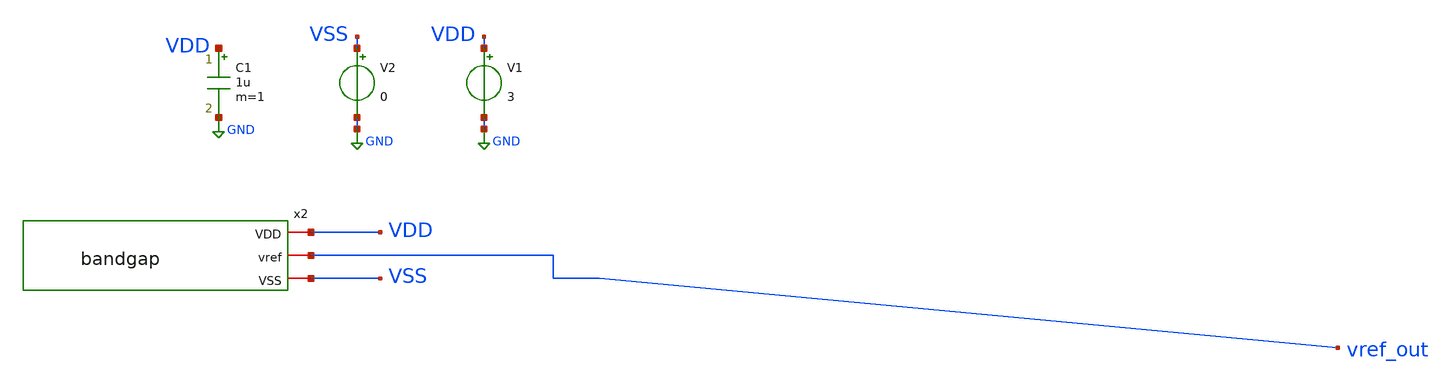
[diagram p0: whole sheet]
** sch_path: xschem/tb_bandgap.sch
**.subckt tb_bandgap
x2 VDD vref_out VSS bandgap
V1 VDD GND 3
V2 VSS GND 0
C1 VDD GND 1u m=1
**** begin user architecture code

** opencircuitdesign pdks install
.lib $::SKYWATER_MODELS/sky130.lib.spice tt





.param top_l = 10
.param top_w = 30
.param top_m = 10

.param mid_l = 10
.param mid_w = 9
.param mid_m = 1

.param bot_l = 2
.param bot_w = 9
.param bot_m = 10

.control

dc v1 3 4 0.1

write bandgap.raw

.endc



**** end user architecture code
**.ends

* expanding   symbol:  bandgap.sym # of pins=3
** sym_path: xschem/bandgap.sym
** sch_path: xschem/bandgap.sch
.subckt bandgap VDD vref VSS
*.iopin VSS
*.iopin VDD
*.iopin vref
XM1 top_gate top_gate VDD VDD sky130_fd_pr__pfet_01v8 L=10 W=10 nf=1 ad='int((nf+1)/2) * W/nf * 0.29'
+ as='int((nf+2)/2) * W/nf * 0.29' pd='2*int((nf+1)/2) * (W/nf + 0.29)' ps='2*int((nf+2)/2) * (W/nf + 0.29)'
+ nrd='0.29 / W' nrs='0.29 / W' sa=0 sb=0 sd=0 mult=1 m=1
XM2 n_gate top_gate VDD VDD sky130_fd_pr__pfet_01v8 L=10 W=10 nf=1 ad='int((nf+1)/2) * W/nf * 0.29' as='int((nf+2)/2) * W/nf * 0.29'
+ pd='2*int((nf+1)/2) * (W/nf + 0.29)' ps='2*int((nf+2)/2) * (W/nf + 0.29)' nrd='0.29 / W' nrs='0.29 / W'
+ sa=0 sb=0 sd=0 mult=1 m=1
XM3 vref top_gate VDD VDD sky130_fd_pr__pfet_01v8 L=10 W=10 nf=1 ad='int((nf+1)/2) * W/nf * 0.29' as='int((nf+2)/2) * W/nf * 0.29'
+ pd='2*int((nf+1)/2) * (W/nf + 0.29)' ps='2*int((nf+2)/2) * (W/nf + 0.29)' nrd='0.29 / W' nrs='0.29 / W'
+ sa=0 sb=0 sd=0 mult=1 m=1
XR4 r4_m6 Va VSS sky130_fd_pr__res_high_po_0p69 L=200 mult=1 m=1
XR1 r1_m8 vref VSS sky130_fd_pr__res_high_po_0p69 L=200 mult=1 m=1
XM9 top_gate n_gate Va VSS sky130_fd_pr__nfet_01v8_lvt L=5 W=10 nf=1 ad='int((nf+1)/2) * W/nf * 0.29'
+ as='int((nf+2)/2) * W/nf * 0.29' pd='2*int((nf+1)/2) * (W/nf + 0.29)' ps='2*int((nf+2)/2) * (W/nf + 0.29)'
+ nrd='0.29 / W' nrs='0.29 / W' sa=0 sb=0 sd=0 mult=1 m=1
XM4 n_gate n_gate Vb VSS sky130_fd_pr__nfet_01v8_lvt L=5 W=10 nf=1 ad='int((nf+1)/2) * W/nf * 0.29' as='int((nf+2)/2) * W/nf * 0.29'
+ pd='2*int((nf+1)/2) * (W/nf + 0.29)' ps='2*int((nf+2)/2) * (W/nf + 0.29)' nrd='0.29 / W' nrs='0.29 / W'
+ sa=0 sb=0 sd=0 mult=1 m=1
XM5 VSS VSS r4_m6 VDD sky130_fd_pr__pfet_01v8_lvt L=5 W=10 nf=1 ad='int((nf+1)/2) * W/nf * 0.29' as='int((nf+2)/2) * W/nf * 0.29'
+ pd='2*int((nf+1)/2) * (W/nf + 0.29)' ps='2*int((nf+2)/2) * (W/nf + 0.29)' nrd='0.29 / W' nrs='0.29 / W'
+ sa=0 sb=0 sd=0 mult=1 m=1
XM6 VSS VSS r1_m8 VDD sky130_fd_pr__pfet_01v8_lvt L=5 W=10 nf=1 ad='int((nf+1)/2) * W/nf * 0.29' as='int((nf+2)/2) * W/nf * 0.29'
+ pd='2*int((nf+1)/2) * (W/nf + 0.29)' ps='2*int((nf+2)/2) * (W/nf + 0.29)' nrd='0.29 / W' nrs='0.29 / W'
+ sa=0 sb=0 sd=0 mult=1 m=1
XM7 VSS VSS Vb VDD sky130_fd_pr__pfet_01v8_lvt L=5 W=3 nf=1 ad='int((nf+1)/2) * W/nf * 0.29' as='int((nf+2)/2) * W/nf * 0.29'
+ pd='2*int((nf+1)/2) * (W/nf + 0.29)' ps='2*int((nf+2)/2) * (W/nf + 0.29)' nrd='0.29 / W' nrs='0.29 / W'
+ sa=0 sb=0 sd=0 mult=1 m=1
.ends

.GLOBAL GND
.end
